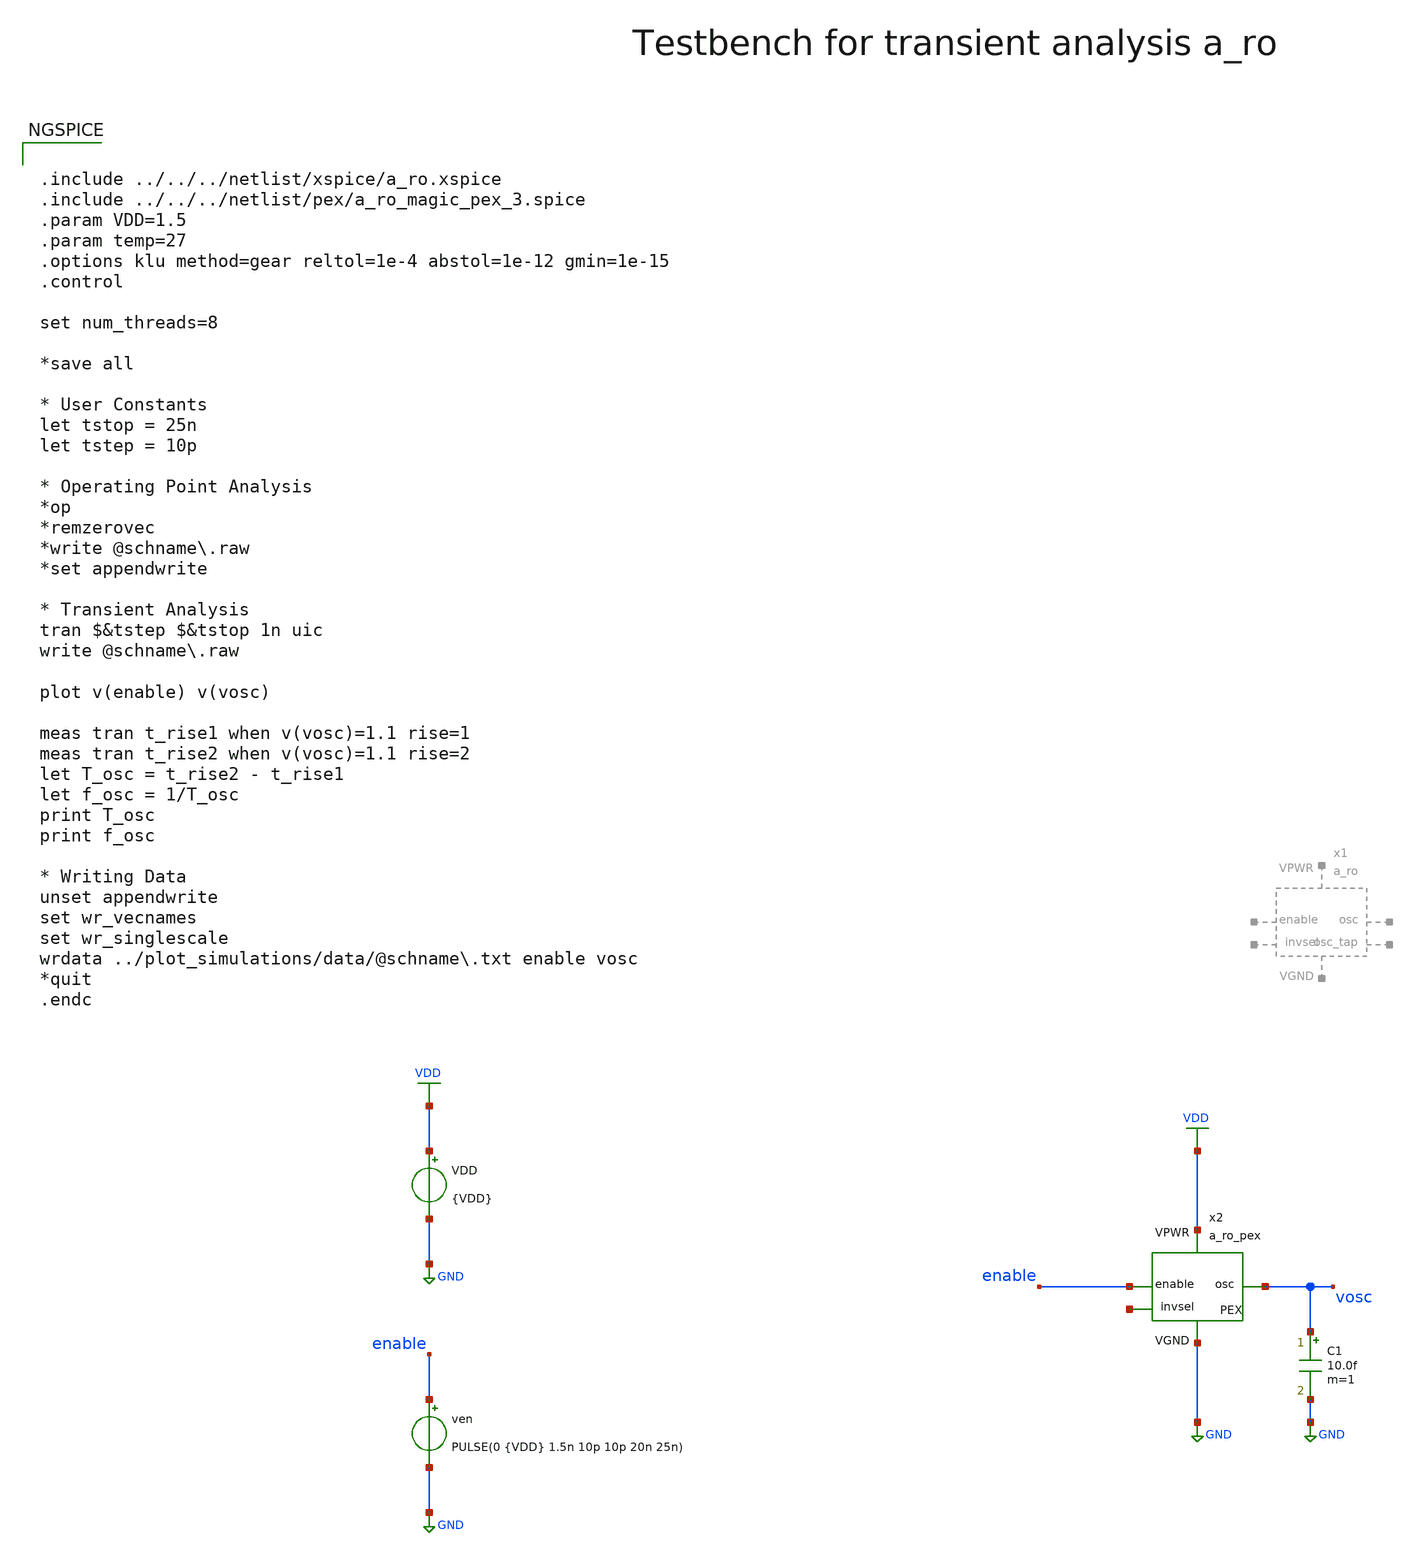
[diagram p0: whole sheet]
** sch_path: macros/heichips26_digital_project/macros/e_load_uniform/testbenches/xschem/e_load_uniform_tb_tran.sch
**.subckt e_load_uniform_tb_tran
VDD VDD GND {VDD}
ven enable GND PULSE(0 {VDD} 1.5n 10p 10p 20n 25n)
x2 VDD GND enable vosc net1[5] net1[4] net1[3] net1[2] net1[1] net1[0] a_ro_pex
C1 vosc GND 10.0f m=1
**** begin user architecture code


.include ../../../netlist/xspice/a_ro.xspice
.include ../../../netlist/pex/a_ro_magic_pex_3.spice
.param VDD=1.5
.param temp=27
.options klu method=gear reltol=1e-4 abstol=1e-12 gmin=1e-15
.control

set num_threads=8

*save all

* User Constants
let tstop = 25n
let tstep = 10p

* Operating Point Analysis
*op
*remzerovec
*write @schname\.raw
*set appendwrite

* Transient Analysis
tran $&tstep $&tstop 1n uic
write @schname\.raw

plot v(enable) v(vosc)

meas tran t_rise1 when v(vosc)=1.1 rise=1
meas tran t_rise2 when v(vosc)=1.1 rise=2
let T_osc = t_rise2 - t_rise1
let f_osc = 1/T_osc
print T_osc
print f_osc

* Writing Data
unset appendwrite
set wr_vecnames
set wr_singlescale
wrdata ../plot_simulations/data/@schname\.txt enable vosc
*quit
.endc


.lib cornerMOSlv.lib mos_tt
.lib cornerMOShv.lib mos_tt
.lib cornerRES.lib res_typ
.lib cornerDIO.lib dio_tt

**** end user architecture code
**.ends
.GLOBAL GND
.GLOBAL VDD
.end
